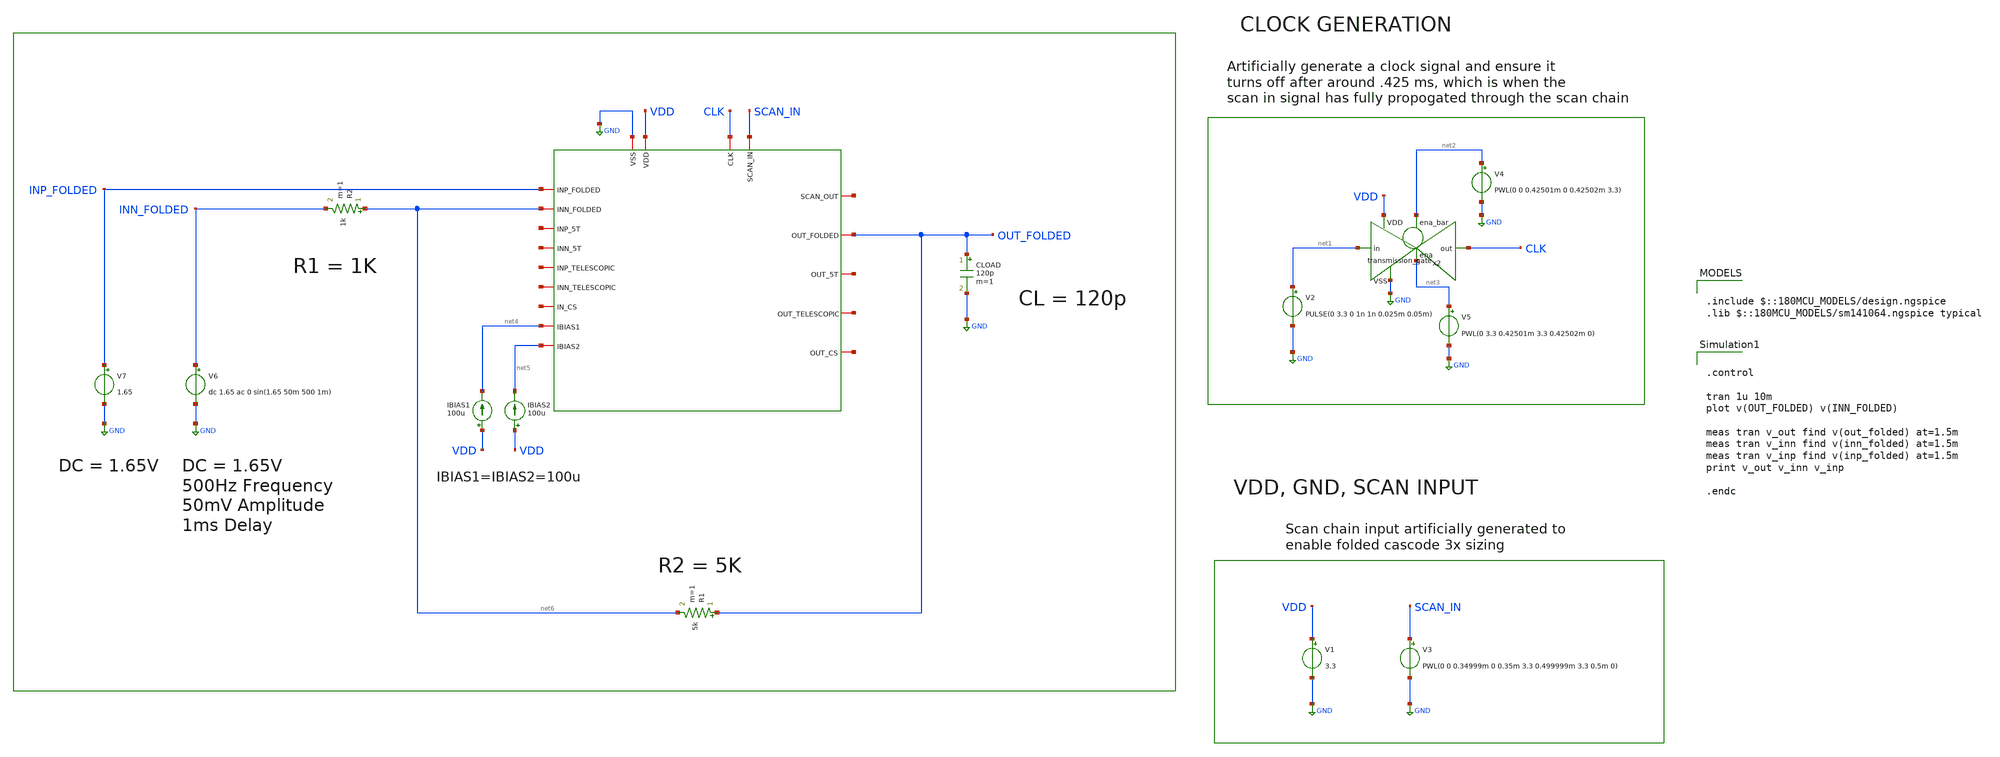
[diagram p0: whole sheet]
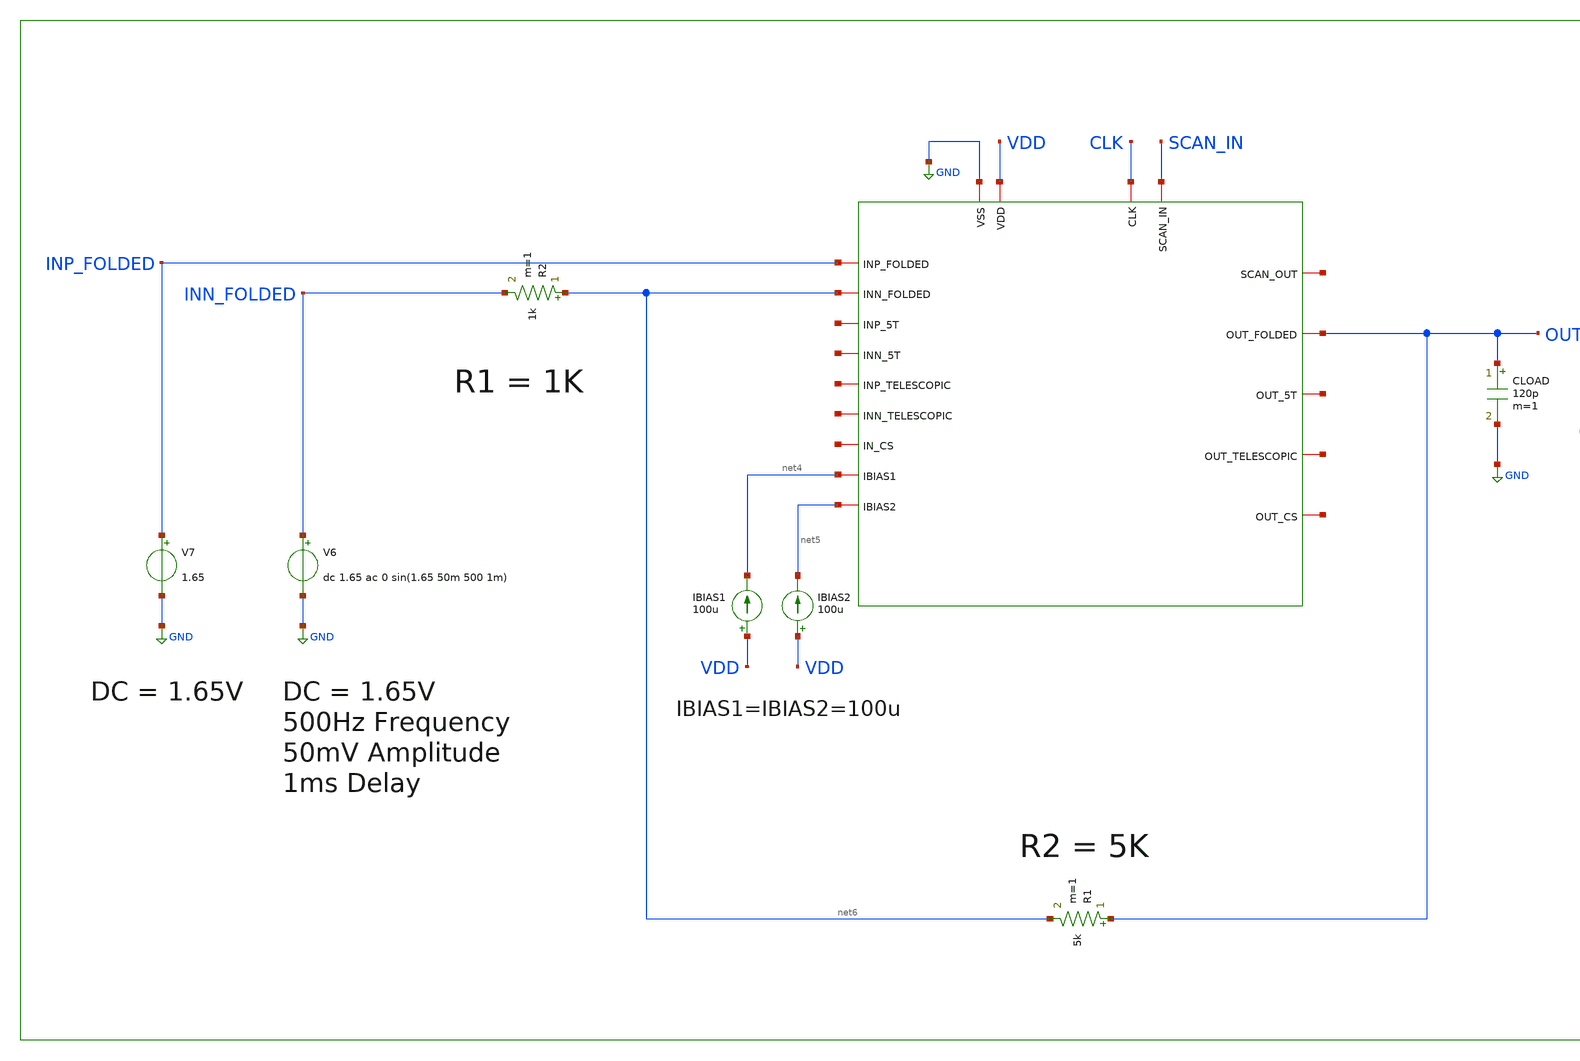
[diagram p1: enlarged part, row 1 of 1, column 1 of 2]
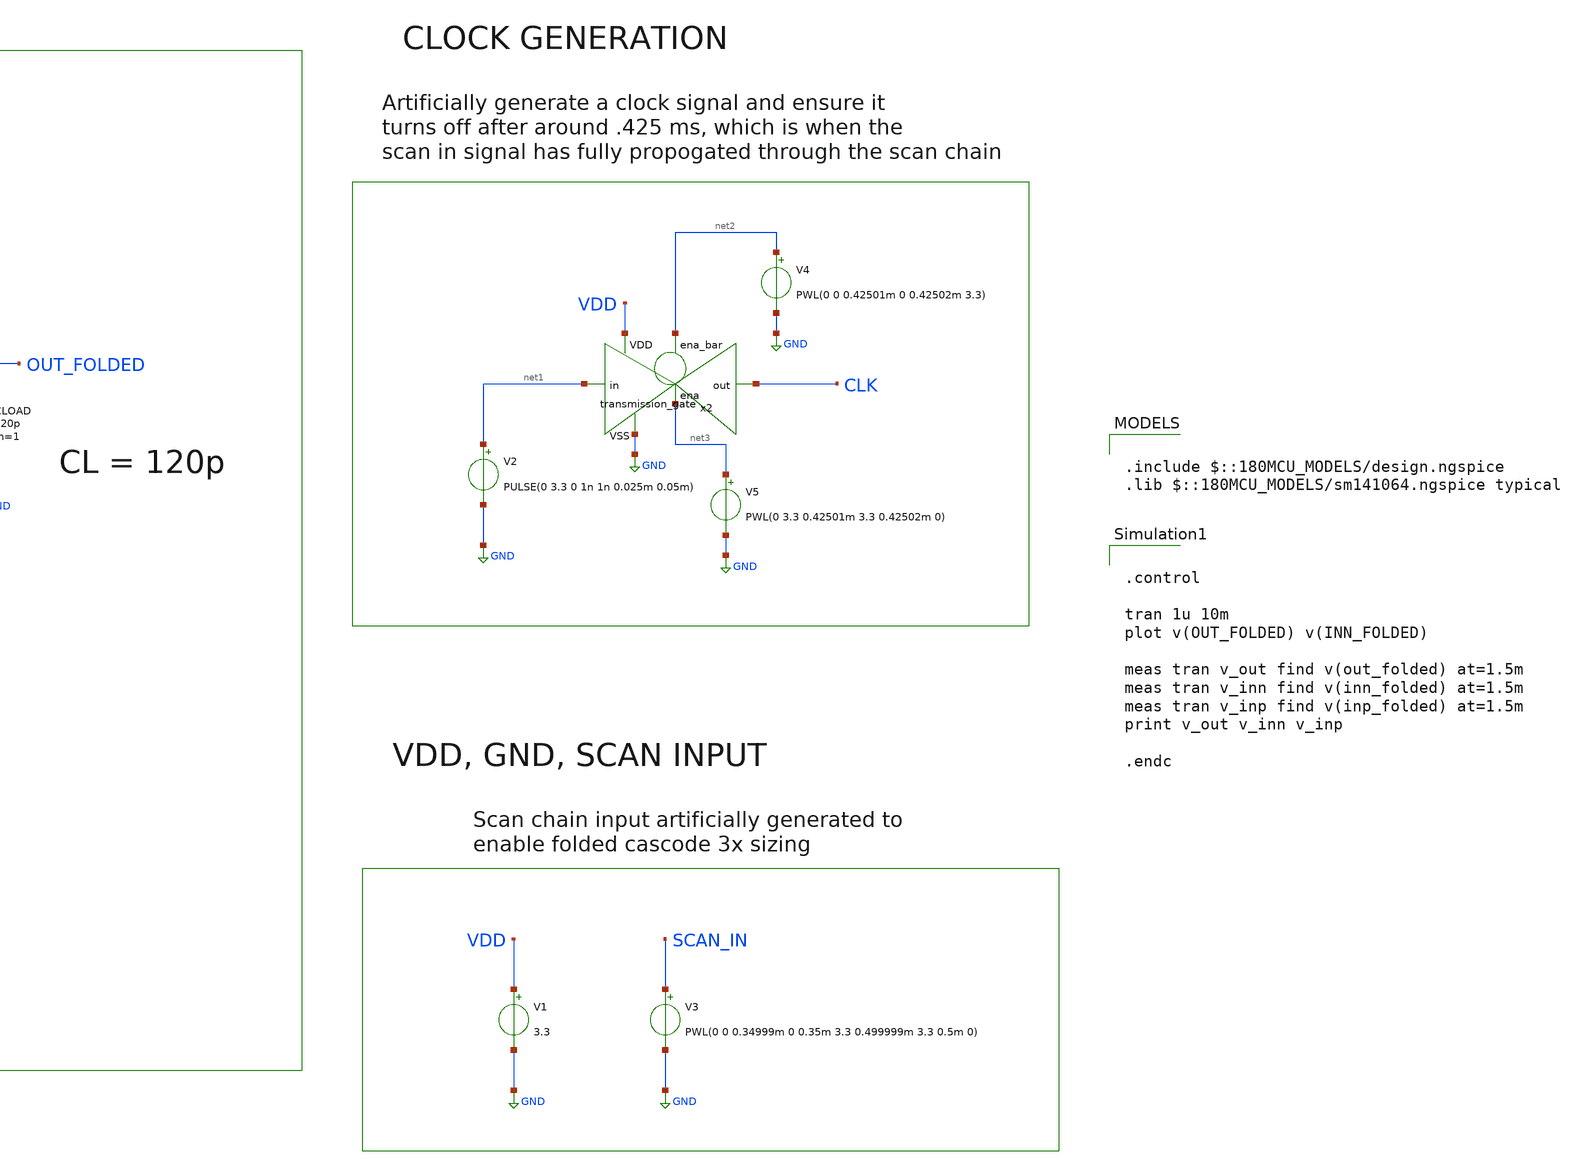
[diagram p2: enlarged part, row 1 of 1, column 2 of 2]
** sch_path: designs/libs/core_tb/system_tb.sch
**.subckt system_tb
x1 CLK net7 SCAN_IN GND VDD OUT_FOLDED INP_FOLDED net8 net5 net4 net6 net9 net10 net11 net12 net13
+ net14 net15 DUT
V3 SCAN_IN GND PWL(0 0 0.34999m 0 0.35m 3.3 0.499999m 3.3 0.5m 0)
V1 VDD GND 3.3
V2 net1 GND PULSE(0 3.3 0 1n 1n 0.025m 0.05m)
x2 net2 VDD CLK net1 GND net3 transmission_gate
V4 net2 GND PWL(0 0 0.42501m 0 0.42502m 3.3)
V5 net3 GND PWL(0 3.3 0.42501m 3.3 0.42502m 0)
IBIAS1 VDD net4 100u
IBIAS2 VDD net5 100u
V7 INP_FOLDED GND 1.65
CLOAD OUT_FOLDED GND 120p m=1
R2 net6 INN_FOLDED 1k m=1
V6 INN_FOLDED GND dc 1.65 ac 0 sin(1.65 50m 500 1m)
R1 OUT_FOLDED net6 5k m=1
**** begin user architecture code

.include $::180MCU_MODELS/design.ngspice
.lib $::180MCU_MODELS/sm141064.ngspice typical



.control

tran 1u 10m
plot v(OUT_FOLDED) v(INN_FOLDED)

meas tran v_out find v(out_folded) at=1.5m
meas tran v_inn find v(inn_folded) at=1.5m
meas tran v_inp find v(inp_folded) at=1.5m
print v_out v_inn v_inp

.endc


**** end user architecture code
**.ends
.GLOBAL GND
.end
